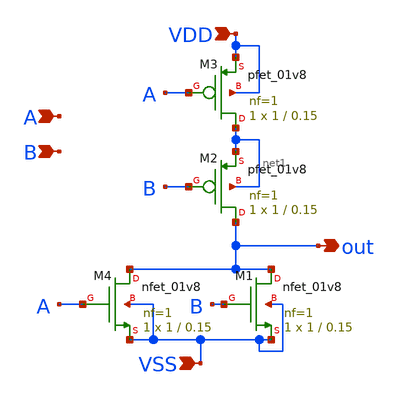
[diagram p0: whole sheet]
** sch_path: nor/nor2.sch
**.subckt nor2 A B out VSS VDD
*.ipin A
*.ipin B
*.opin out
*.ipin VSS
*.ipin VDD
XM1 out B VSS VSS sky130_fd_pr__nfet_01v8 L=0.15 W=1 nf=1 ad='int((nf+1)/2) * W/nf * 0.29' as='int((nf+2)/2) * W/nf * 0.29'
+ pd='2*int((nf+1)/2) * (W/nf + 0.29)' ps='2*int((nf+2)/2) * (W/nf + 0.29)' nrd='0.29 / W' nrs='0.29 / W'
+ sa=0 sb=0 sd=0 mult=1 m=1
XM2 out B net1 net1 sky130_fd_pr__pfet_01v8 L=0.15 W=1 nf=1 ad='int((nf+1)/2) * W/nf * 0.29' as='int((nf+2)/2) * W/nf * 0.29'
+ pd='2*int((nf+1)/2) * (W/nf + 0.29)' ps='2*int((nf+2)/2) * (W/nf + 0.29)' nrd='0.29 / W' nrs='0.29 / W'
+ sa=0 sb=0 sd=0 mult=1 m=1
XM3 net1 A VDD VDD sky130_fd_pr__pfet_01v8 L=0.15 W=1 nf=1 ad='int((nf+1)/2) * W/nf * 0.29' as='int((nf+2)/2) * W/nf * 0.29'
+ pd='2*int((nf+1)/2) * (W/nf + 0.29)' ps='2*int((nf+2)/2) * (W/nf + 0.29)' nrd='0.29 / W' nrs='0.29 / W'
+ sa=0 sb=0 sd=0 mult=1 m=1
XM4 out A VSS VSS sky130_fd_pr__nfet_01v8 L=0.15 W=1 nf=1 ad='int((nf+1)/2) * W/nf * 0.29' as='int((nf+2)/2) * W/nf * 0.29'
+ pd='2*int((nf+1)/2) * (W/nf + 0.29)' ps='2*int((nf+2)/2) * (W/nf + 0.29)' nrd='0.29 / W' nrs='0.29 / W'
+ sa=0 sb=0 sd=0 mult=1 m=1
**.ends
.end
